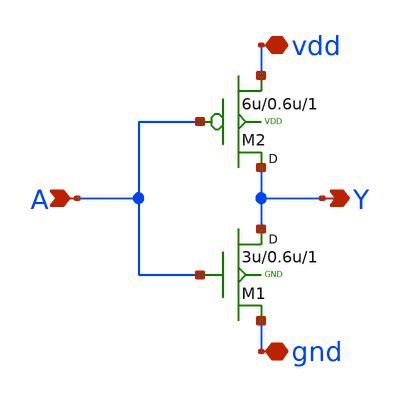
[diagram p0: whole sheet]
** sch_path: Tutorials/1-4_StdCell_DFFSR/Sch/INVX1.sch
**.subckt INVX1 A Y vdd gnd
*.ipin A
*.opin Y
*.iopin vdd
*.iopin gnd
M1 Y A gnd GND nfet w=3u l=0.6u m=1
M2 Y A vdd VDD pfet w=6u l=0.6u m=1
**.ends
.end
